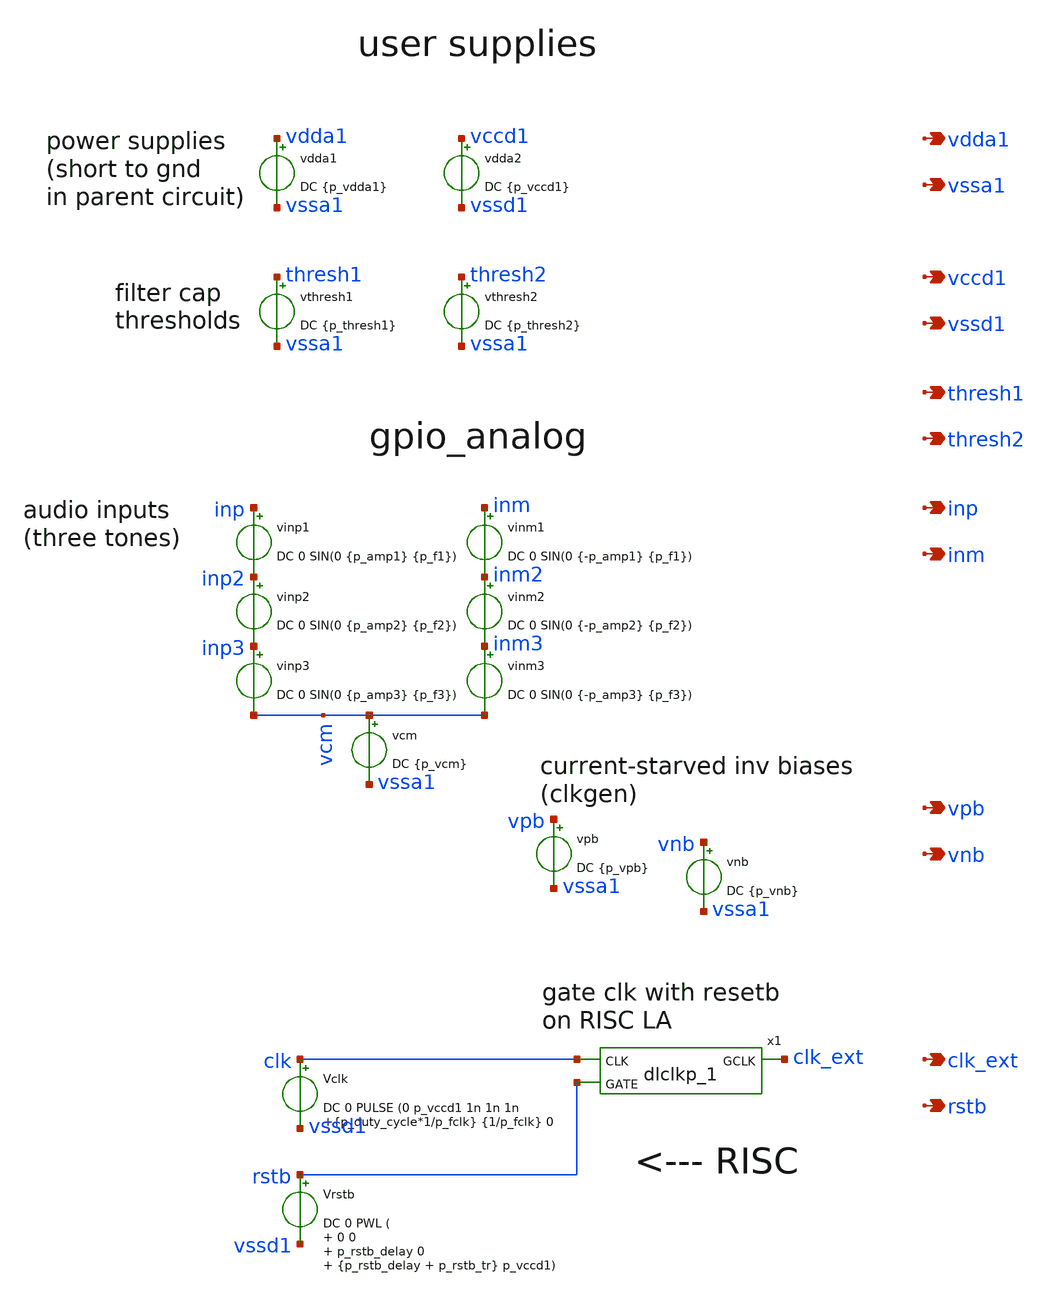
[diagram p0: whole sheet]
** sch_path: xschem/test_bench/pad_frame.sch
**.subckt pad_frame thresh1 thresh2 vdda1 vssa1 inp inm vccd1 vssd1 rstb clk_ext vpb vnb
*.opin thresh1
*.opin thresh2
*.opin vdda1
*.opin vssa1
*.opin inp
*.opin inm
*.opin vccd1
*.opin vssd1
*.opin rstb
*.opin clk_ext
*.opin vpb
*.opin vnb
vdda1 vdda1 vssa1 DC {p_vdda1}
vthresh1 thresh1 vssa1 DC {p_thresh1}
vthresh2 thresh2 vssa1 DC {p_thresh2}
vinp1 inp inp2 DC 0 SIN(0 {p_amp1} {p_f1})
vinm1 inm inm2 DC 0 SIN(0 {-p_amp1} {p_f1})
vpb vpb vssa1 DC {p_vpb}
vnb vnb vssa1 DC {p_vnb}
vinp2 inp2 inp3 DC 0 SIN(0 {p_amp2} {p_f2})
vinp3 inp3 vcm DC 0 SIN(0 {p_amp3} {p_f3})
vinm2 inm2 inm3 DC 0 SIN(0 {-p_amp2} {p_f2})
vinm3 inm3 vcm DC 0 SIN(0 {-p_amp3} {p_f3})
vcm vcm vssa1 DC {p_vcm}
vdda2 vccd1 vssd1 DC {p_vccd1}
Vclk clk vssd1 DC 0 PULSE (0 p_vccd1 1n 1n 1n {p_duty_cycle*1/p_fclk} {1/p_fclk} 0
Vrstb rstb vssd1 DC 0 PWL ( 0 0 p_rstb_delay 0 {p_rstb_delay + p_rstb_tr} p_vccd1)
x1 clk rstb vssd1 vssd1 vccd1 vccd1 clk_ext sky130_fd_sc_hd__dlclkp_1
**.ends
.end
